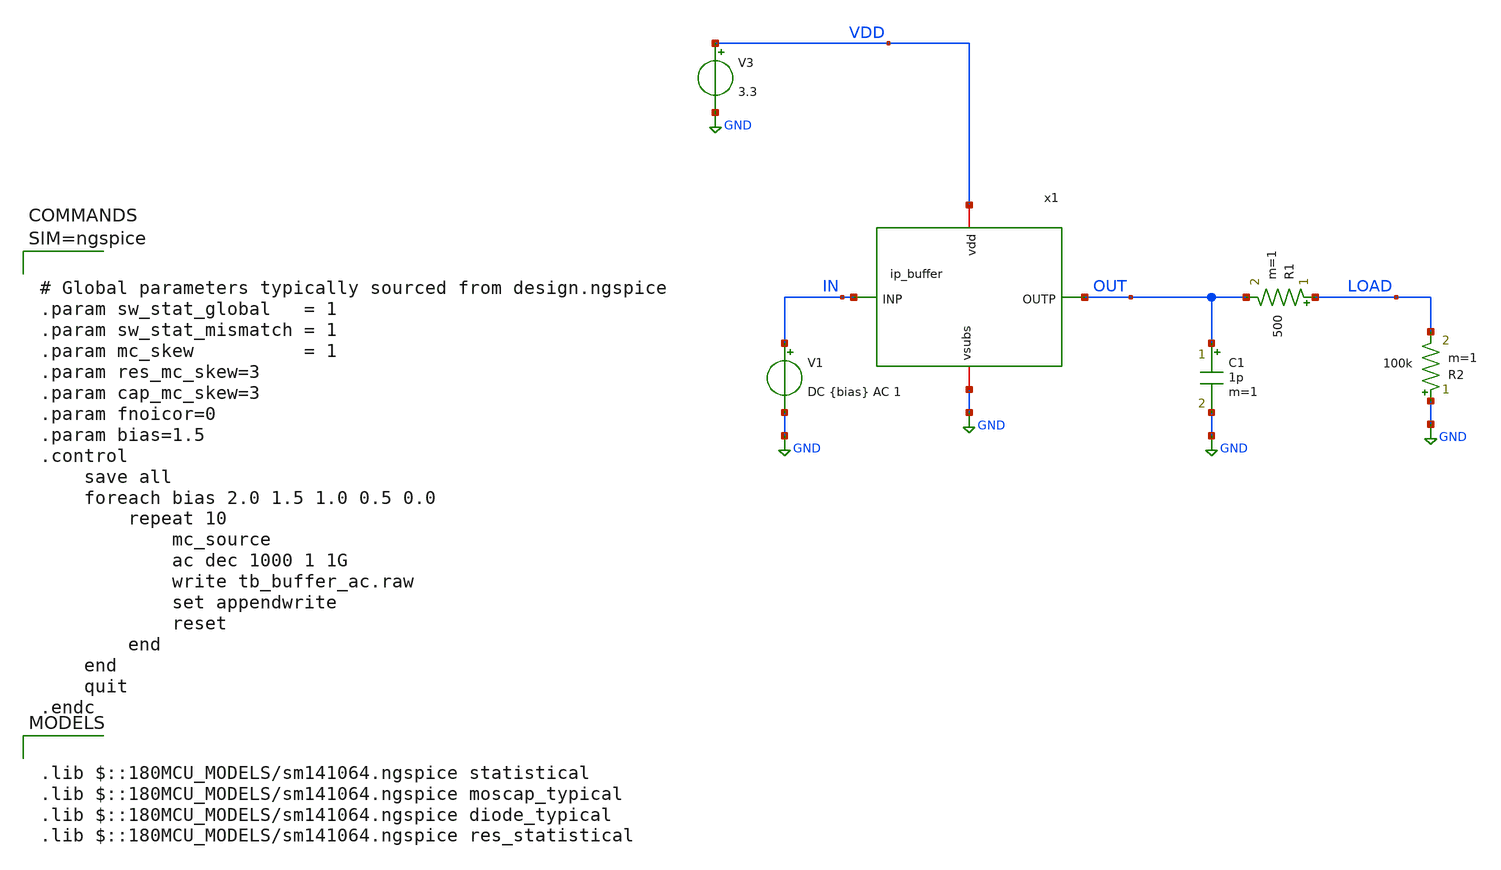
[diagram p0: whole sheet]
** sch_path: xschem/tb_buffer_ac.sch
**.subckt tb_buffer_ac
x1 VDD OUT IN GND ip_buffer
V3 VDD GND 3.3
V1 IN GND DC {bias} AC 1
R1 LOAD OUT 500 m=1
C1 OUT GND 1p m=1
R2 GND LOAD 100k m=1
**** begin user architecture code

.lib $::180MCU_MODELS/sm141064.ngspice statistical
.lib $::180MCU_MODELS/sm141064.ngspice moscap_typical
.lib $::180MCU_MODELS/sm141064.ngspice diode_typical
.lib $::180MCU_MODELS/sm141064.ngspice res_statistical




# Global parameters typically sourced from design.ngspice
.param sw_stat_global   = 1
.param sw_stat_mismatch = 1
.param mc_skew          = 1
.param res_mc_skew=3
.param cap_mc_skew=3
.param fnoicor=0
.param bias=1.5
.control
	save all
	foreach bias 2.0 1.5 1.0 0.5 0.0
		repeat 10
			mc_source
			ac dec 1000 1 1G
			write tb_buffer_ac.raw
			set appendwrite
			reset
		end
	end
	quit
.endc



**** end user architecture code
**.ends

* expanding   symbol:  ip_buffer.sym # of pins=4
** sym_path: xschem/ip_buffer.sym
** sch_path: xschem/ip_buffer.sch
.subckt ip_buffer vdd OUTP INP vsubs
*.iopin vsubs
*.iopin vdd
*.ipin INP
*.opin OUTP
XM1 vsubs INP OUTP OUTP pfet_06v0 L=1u W=10u nf=1 ad='int((nf+1)/2) * W/nf * 0.18u' as='int((nf+2)/2) * W/nf * 0.18u'
+ pd='2*int((nf+1)/2) * (W/nf + 0.18u)' ps='2*int((nf+2)/2) * (W/nf + 0.18u)' nrd='0.18u / W' nrs='0.18u / W'
+ sa=0 sb=0 sd=0 m=15
R1 net2 vsubs 36k m=1
Vmeas net1 net2 0
XM4 OUTP net1 vdd vdd pfet_06v0 L=2u W=10u nf=1 ad='int((nf+1)/2) * W/nf * 0.18u' as='int((nf+2)/2) * W/nf * 0.18u'
+ pd='2*int((nf+1)/2) * (W/nf + 0.18u)' ps='2*int((nf+2)/2) * (W/nf + 0.18u)' nrd='0.18u / W' nrs='0.18u / W'
+ sa=0 sb=0 sd=0 m=5
XM2 net1 net1 vdd vdd pfet_06v0 L=2u W=10u nf=1 ad='int((nf+1)/2) * W/nf * 0.18u' as='int((nf+2)/2) * W/nf * 0.18u'
+ pd='2*int((nf+1)/2) * (W/nf + 0.18u)' ps='2*int((nf+2)/2) * (W/nf + 0.18u)' nrd='0.18u / W' nrs='0.18u / W'
+ sa=0 sb=0 sd=0 m=3
.ends

.GLOBAL GND
.end
